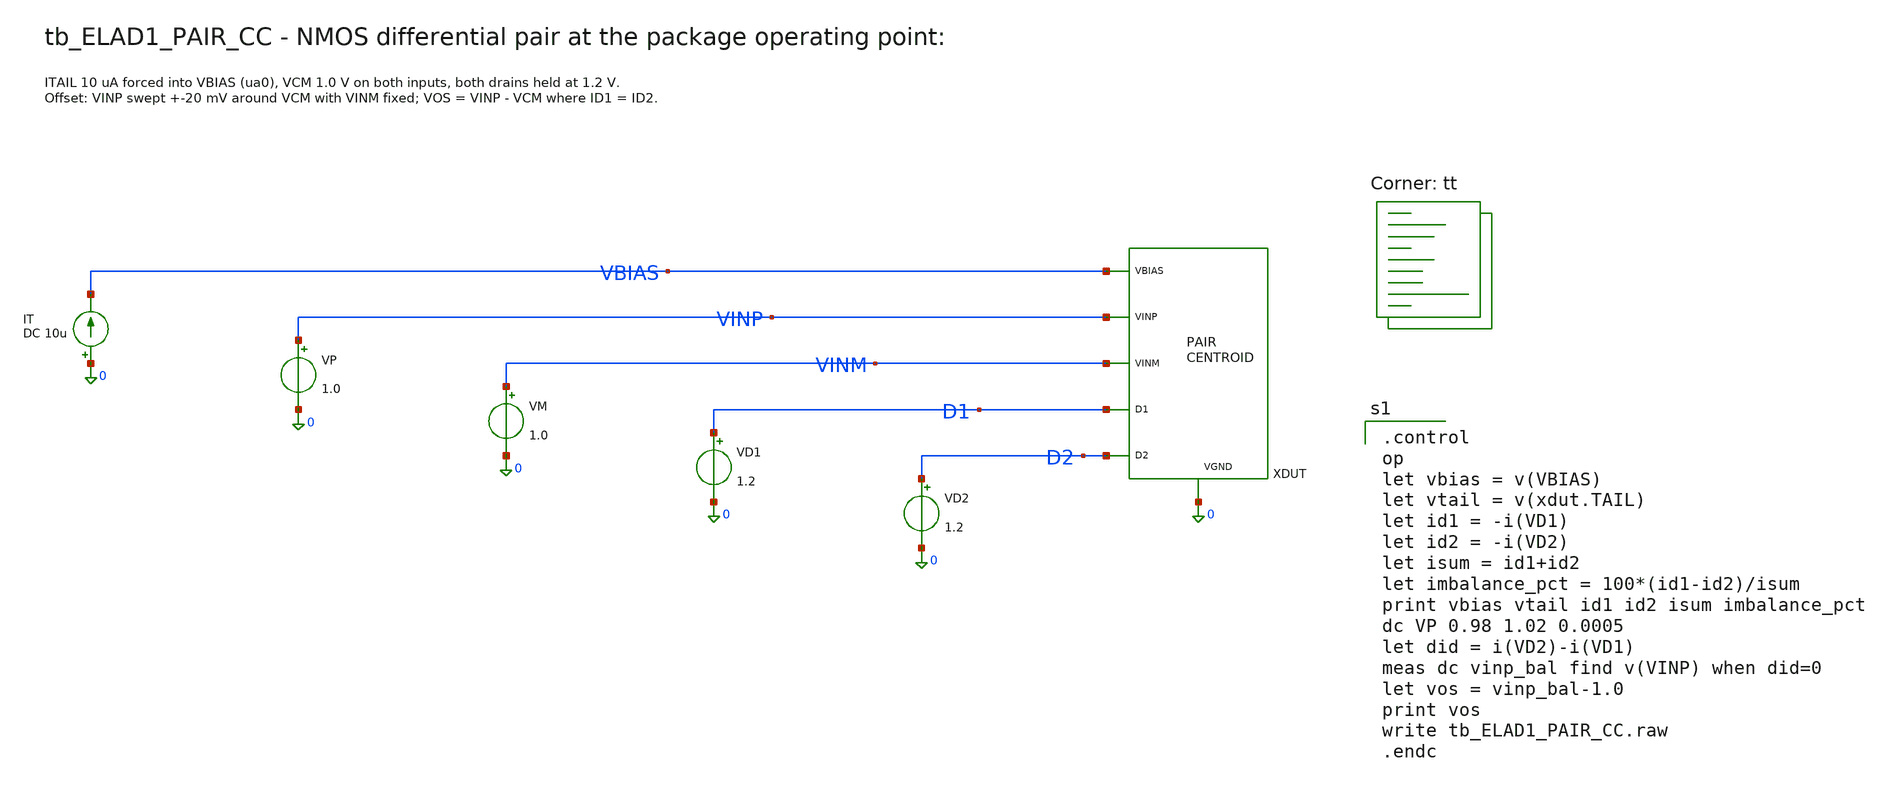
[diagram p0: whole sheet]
** sch_path: cells/ELAD1_PAIR_CC/schematic/tb_ELAD1_PAIR_CC.sch
**.subckt tb_ELAD1_PAIR_CC
XDUT VINP VINM D1 D2 VBIAS 0 ELAD1_PAIR_CC
VD2 D2 0 1.2
VD1 D1 0 1.2
VM VINM 0 1.0
VP VINP 0 1.0
IT 0 VBIAS DC 10u
**** begin user architecture code

.control
op
let vbias = v(VBIAS)
let vtail = v(xdut.TAIL)
let id1 = -i(VD1)
let id2 = -i(VD2)
let isum = id1+id2
let imbalance_pct = 100*(id1-id2)/isum
print vbias vtail id1 id2 isum imbalance_pct
dc VP 0.98 1.02 0.0005
let did = i(VD2)-i(VD1)
meas dc vinp_bal find v(VINP) when did=0
let vos = vinp_bal-1.0
print vos
write tb_ELAD1_PAIR_CC.raw
.endc

.lib $::SKYWATER_MODELS/sky130.lib.spice tt
**** end user architecture code
**.ends

* expanding   symbol:  ELAD1_PAIR_CC.sym # of pins=6
** sym_path: cells/ELAD1_PAIR_CC/schematic/ELAD1_PAIR_CC.sym
** sch_path: cells/ELAD1_PAIR_CC/schematic/ELAD1_PAIR_CC.sch
.subckt ELAD1_PAIR_CC VINP VINM D1 D2 VBIAS VGND
*.iopin D1
*.iopin D2
*.iopin VINP
*.iopin VINM
*.iopin VBIAS
*.iopin VGND
XA[3] D1 VINP TAIL VGND sky130_fd_pr__nfet_01v8 L=1 W=2 nf=1 ad='int((1 + 1)/2) * 2 / 1 * 0.29' as='int((1 + 2)/2) * 2 / 1 * 0.29'
+ pd='2*int((1 + 1)/2) * (2 / 1 + 0.29)' ps='2*int((1 + 2)/2) * (2 / 1 + 0.29)' nrd='0.29 / 2 ' nrs='0.29 / 2 '
+ sa=0 sb=0 sd=0 mult=1 m=1
XA[2] D1 VINP TAIL VGND sky130_fd_pr__nfet_01v8 L=1 W=2 nf=1 ad='int((1 + 1)/2) * 2 / 1 * 0.29' as='int((1 + 2)/2) * 2 / 1 * 0.29'
+ pd='2*int((1 + 1)/2) * (2 / 1 + 0.29)' ps='2*int((1 + 2)/2) * (2 / 1 + 0.29)' nrd='0.29 / 2 ' nrs='0.29 / 2 '
+ sa=0 sb=0 sd=0 mult=1 m=1
XA[1] D1 VINP TAIL VGND sky130_fd_pr__nfet_01v8 L=1 W=2 nf=1 ad='int((1 + 1)/2) * 2 / 1 * 0.29' as='int((1 + 2)/2) * 2 / 1 * 0.29'
+ pd='2*int((1 + 1)/2) * (2 / 1 + 0.29)' ps='2*int((1 + 2)/2) * (2 / 1 + 0.29)' nrd='0.29 / 2 ' nrs='0.29 / 2 '
+ sa=0 sb=0 sd=0 mult=1 m=1
XA[0] D1 VINP TAIL VGND sky130_fd_pr__nfet_01v8 L=1 W=2 nf=1 ad='int((1 + 1)/2) * 2 / 1 * 0.29' as='int((1 + 2)/2) * 2 / 1 * 0.29'
+ pd='2*int((1 + 1)/2) * (2 / 1 + 0.29)' ps='2*int((1 + 2)/2) * (2 / 1 + 0.29)' nrd='0.29 / 2 ' nrs='0.29 / 2 '
+ sa=0 sb=0 sd=0 mult=1 m=1
XB[3] D2 VINM TAIL VGND sky130_fd_pr__nfet_01v8 L=1 W=2 nf=1 ad='int((1 + 1)/2) * 2 / 1 * 0.29' as='int((1 + 2)/2) * 2 / 1 * 0.29'
+ pd='2*int((1 + 1)/2) * (2 / 1 + 0.29)' ps='2*int((1 + 2)/2) * (2 / 1 + 0.29)' nrd='0.29 / 2 ' nrs='0.29 / 2 '
+ sa=0 sb=0 sd=0 mult=1 m=1
XB[2] D2 VINM TAIL VGND sky130_fd_pr__nfet_01v8 L=1 W=2 nf=1 ad='int((1 + 1)/2) * 2 / 1 * 0.29' as='int((1 + 2)/2) * 2 / 1 * 0.29'
+ pd='2*int((1 + 1)/2) * (2 / 1 + 0.29)' ps='2*int((1 + 2)/2) * (2 / 1 + 0.29)' nrd='0.29 / 2 ' nrs='0.29 / 2 '
+ sa=0 sb=0 sd=0 mult=1 m=1
XB[1] D2 VINM TAIL VGND sky130_fd_pr__nfet_01v8 L=1 W=2 nf=1 ad='int((1 + 1)/2) * 2 / 1 * 0.29' as='int((1 + 2)/2) * 2 / 1 * 0.29'
+ pd='2*int((1 + 1)/2) * (2 / 1 + 0.29)' ps='2*int((1 + 2)/2) * (2 / 1 + 0.29)' nrd='0.29 / 2 ' nrs='0.29 / 2 '
+ sa=0 sb=0 sd=0 mult=1 m=1
XB[0] D2 VINM TAIL VGND sky130_fd_pr__nfet_01v8 L=1 W=2 nf=1 ad='int((1 + 1)/2) * 2 / 1 * 0.29' as='int((1 + 2)/2) * 2 / 1 * 0.29'
+ pd='2*int((1 + 1)/2) * (2 / 1 + 0.29)' ps='2*int((1 + 2)/2) * (2 / 1 + 0.29)' nrd='0.29 / 2 ' nrs='0.29 / 2 '
+ sa=0 sb=0 sd=0 mult=1 m=1
XT[3] TAIL VBIAS VGND VGND sky130_fd_pr__nfet_01v8 L=1 W=2 nf=1 ad='int((1 + 1)/2) * 2 / 1 * 0.29' as='int((1 + 2)/2) * 2 / 1 * 0.29'
+ pd='2*int((1 + 1)/2) * (2 / 1 + 0.29)' ps='2*int((1 + 2)/2) * (2 / 1 + 0.29)' nrd='0.29 / 2 ' nrs='0.29 / 2 '
+ sa=0 sb=0 sd=0 mult=1 m=1
XT[2] TAIL VBIAS VGND VGND sky130_fd_pr__nfet_01v8 L=1 W=2 nf=1 ad='int((1 + 1)/2) * 2 / 1 * 0.29' as='int((1 + 2)/2) * 2 / 1 * 0.29'
+ pd='2*int((1 + 1)/2) * (2 / 1 + 0.29)' ps='2*int((1 + 2)/2) * (2 / 1 + 0.29)' nrd='0.29 / 2 ' nrs='0.29 / 2 '
+ sa=0 sb=0 sd=0 mult=1 m=1
XT[1] TAIL VBIAS VGND VGND sky130_fd_pr__nfet_01v8 L=1 W=2 nf=1 ad='int((1 + 1)/2) * 2 / 1 * 0.29' as='int((1 + 2)/2) * 2 / 1 * 0.29'
+ pd='2*int((1 + 1)/2) * (2 / 1 + 0.29)' ps='2*int((1 + 2)/2) * (2 / 1 + 0.29)' nrd='0.29 / 2 ' nrs='0.29 / 2 '
+ sa=0 sb=0 sd=0 mult=1 m=1
XT[0] TAIL VBIAS VGND VGND sky130_fd_pr__nfet_01v8 L=1 W=2 nf=1 ad='int((1 + 1)/2) * 2 / 1 * 0.29' as='int((1 + 2)/2) * 2 / 1 * 0.29'
+ pd='2*int((1 + 1)/2) * (2 / 1 + 0.29)' ps='2*int((1 + 2)/2) * (2 / 1 + 0.29)' nrd='0.29 / 2 ' nrs='0.29 / 2 '
+ sa=0 sb=0 sd=0 mult=1 m=1
XR[3] VBIAS VBIAS VGND VGND sky130_fd_pr__nfet_01v8 L=1 W=2 nf=1 ad='int((1 + 1)/2) * 2 / 1 * 0.29' as='int((1 + 2)/2) * 2 / 1 * 0.29'
+ pd='2*int((1 + 1)/2) * (2 / 1 + 0.29)' ps='2*int((1 + 2)/2) * (2 / 1 + 0.29)' nrd='0.29 / 2 ' nrs='0.29 / 2 '
+ sa=0 sb=0 sd=0 mult=1 m=1
XR[2] VBIAS VBIAS VGND VGND sky130_fd_pr__nfet_01v8 L=1 W=2 nf=1 ad='int((1 + 1)/2) * 2 / 1 * 0.29' as='int((1 + 2)/2) * 2 / 1 * 0.29'
+ pd='2*int((1 + 1)/2) * (2 / 1 + 0.29)' ps='2*int((1 + 2)/2) * (2 / 1 + 0.29)' nrd='0.29 / 2 ' nrs='0.29 / 2 '
+ sa=0 sb=0 sd=0 mult=1 m=1
XR[1] VBIAS VBIAS VGND VGND sky130_fd_pr__nfet_01v8 L=1 W=2 nf=1 ad='int((1 + 1)/2) * 2 / 1 * 0.29' as='int((1 + 2)/2) * 2 / 1 * 0.29'
+ pd='2*int((1 + 1)/2) * (2 / 1 + 0.29)' ps='2*int((1 + 2)/2) * (2 / 1 + 0.29)' nrd='0.29 / 2 ' nrs='0.29 / 2 '
+ sa=0 sb=0 sd=0 mult=1 m=1
XR[0] VBIAS VBIAS VGND VGND sky130_fd_pr__nfet_01v8 L=1 W=2 nf=1 ad='int((1 + 1)/2) * 2 / 1 * 0.29' as='int((1 + 2)/2) * 2 / 1 * 0.29'
+ pd='2*int((1 + 1)/2) * (2 / 1 + 0.29)' ps='2*int((1 + 2)/2) * (2 / 1 + 0.29)' nrd='0.29 / 2 ' nrs='0.29 / 2 '
+ sa=0 sb=0 sd=0 mult=1 m=1
XDUM[31] VGND VGND VGND VGND sky130_fd_pr__nfet_01v8 L=1 W=2 nf=1 ad='int((1 + 1)/2) * 2 / 1 * 0.29'
+ as='int((1 + 2)/2) * 2 / 1 * 0.29' pd='2*int((1 + 1)/2) * (2 / 1 + 0.29)' ps='2*int((1 + 2)/2) * (2 / 1 + 0.29)'
+ nrd='0.29 / 2 ' nrs='0.29 / 2 ' sa=0 sb=0 sd=0 mult=1 m=1
XDUM[30] VGND VGND VGND VGND sky130_fd_pr__nfet_01v8 L=1 W=2 nf=1 ad='int((1 + 1)/2) * 2 / 1 * 0.29'
+ as='int((1 + 2)/2) * 2 / 1 * 0.29' pd='2*int((1 + 1)/2) * (2 / 1 + 0.29)' ps='2*int((1 + 2)/2) * (2 / 1 + 0.29)'
+ nrd='0.29 / 2 ' nrs='0.29 / 2 ' sa=0 sb=0 sd=0 mult=1 m=1
XDUM[29] VGND VGND VGND VGND sky130_fd_pr__nfet_01v8 L=1 W=2 nf=1 ad='int((1 + 1)/2) * 2 / 1 * 0.29'
+ as='int((1 + 2)/2) * 2 / 1 * 0.29' pd='2*int((1 + 1)/2) * (2 / 1 + 0.29)' ps='2*int((1 + 2)/2) * (2 / 1 + 0.29)'
+ nrd='0.29 / 2 ' nrs='0.29 / 2 ' sa=0 sb=0 sd=0 mult=1 m=1
XDUM[28] VGND VGND VGND VGND sky130_fd_pr__nfet_01v8 L=1 W=2 nf=1 ad='int((1 + 1)/2) * 2 / 1 * 0.29'
+ as='int((1 + 2)/2) * 2 / 1 * 0.29' pd='2*int((1 + 1)/2) * (2 / 1 + 0.29)' ps='2*int((1 + 2)/2) * (2 / 1 + 0.29)'
+ nrd='0.29 / 2 ' nrs='0.29 / 2 ' sa=0 sb=0 sd=0 mult=1 m=1
XDUM[27] VGND VGND VGND VGND sky130_fd_pr__nfet_01v8 L=1 W=2 nf=1 ad='int((1 + 1)/2) * 2 / 1 * 0.29'
+ as='int((1 + 2)/2) * 2 / 1 * 0.29' pd='2*int((1 + 1)/2) * (2 / 1 + 0.29)' ps='2*int((1 + 2)/2) * (2 / 1 + 0.29)'
+ nrd='0.29 / 2 ' nrs='0.29 / 2 ' sa=0 sb=0 sd=0 mult=1 m=1
XDUM[26] VGND VGND VGND VGND sky130_fd_pr__nfet_01v8 L=1 W=2 nf=1 ad='int((1 + 1)/2) * 2 / 1 * 0.29'
+ as='int((1 + 2)/2) * 2 / 1 * 0.29' pd='2*int((1 + 1)/2) * (2 / 1 + 0.29)' ps='2*int((1 + 2)/2) * (2 / 1 + 0.29)'
+ nrd='0.29 / 2 ' nrs='0.29 / 2 ' sa=0 sb=0 sd=0 mult=1 m=1
XDUM[25] VGND VGND VGND VGND sky130_fd_pr__nfet_01v8 L=1 W=2 nf=1 ad='int((1 + 1)/2) * 2 / 1 * 0.29'
+ as='int((1 + 2)/2) * 2 / 1 * 0.29' pd='2*int((1 + 1)/2) * (2 / 1 + 0.29)' ps='2*int((1 + 2)/2) * (2 / 1 + 0.29)'
+ nrd='0.29 / 2 ' nrs='0.29 / 2 ' sa=0 sb=0 sd=0 mult=1 m=1
XDUM[24] VGND VGND VGND VGND sky130_fd_pr__nfet_01v8 L=1 W=2 nf=1 ad='int((1 + 1)/2) * 2 / 1 * 0.29'
+ as='int((1 + 2)/2) * 2 / 1 * 0.29' pd='2*int((1 + 1)/2) * (2 / 1 + 0.29)' ps='2*int((1 + 2)/2) * (2 / 1 + 0.29)'
+ nrd='0.29 / 2 ' nrs='0.29 / 2 ' sa=0 sb=0 sd=0 mult=1 m=1
XDUM[23] VGND VGND VGND VGND sky130_fd_pr__nfet_01v8 L=1 W=2 nf=1 ad='int((1 + 1)/2) * 2 / 1 * 0.29'
+ as='int((1 + 2)/2) * 2 / 1 * 0.29' pd='2*int((1 + 1)/2) * (2 / 1 + 0.29)' ps='2*int((1 + 2)/2) * (2 / 1 + 0.29)'
+ nrd='0.29 / 2 ' nrs='0.29 / 2 ' sa=0 sb=0 sd=0 mult=1 m=1
XDUM[22] VGND VGND VGND VGND sky130_fd_pr__nfet_01v8 L=1 W=2 nf=1 ad='int((1 + 1)/2) * 2 / 1 * 0.29'
+ as='int((1 + 2)/2) * 2 / 1 * 0.29' pd='2*int((1 + 1)/2) * (2 / 1 + 0.29)' ps='2*int((1 + 2)/2) * (2 / 1 + 0.29)'
+ nrd='0.29 / 2 ' nrs='0.29 / 2 ' sa=0 sb=0 sd=0 mult=1 m=1
XDUM[21] VGND VGND VGND VGND sky130_fd_pr__nfet_01v8 L=1 W=2 nf=1 ad='int((1 + 1)/2) * 2 / 1 * 0.29'
+ as='int((1 + 2)/2) * 2 / 1 * 0.29' pd='2*int((1 + 1)/2) * (2 / 1 + 0.29)' ps='2*int((1 + 2)/2) * (2 / 1 + 0.29)'
+ nrd='0.29 / 2 ' nrs='0.29 / 2 ' sa=0 sb=0 sd=0 mult=1 m=1
XDUM[20] VGND VGND VGND VGND sky130_fd_pr__nfet_01v8 L=1 W=2 nf=1 ad='int((1 + 1)/2) * 2 / 1 * 0.29'
+ as='int((1 + 2)/2) * 2 / 1 * 0.29' pd='2*int((1 + 1)/2) * (2 / 1 + 0.29)' ps='2*int((1 + 2)/2) * (2 / 1 + 0.29)'
+ nrd='0.29 / 2 ' nrs='0.29 / 2 ' sa=0 sb=0 sd=0 mult=1 m=1
XDUM[19] VGND VGND VGND VGND sky130_fd_pr__nfet_01v8 L=1 W=2 nf=1 ad='int((1 + 1)/2) * 2 / 1 * 0.29'
+ as='int((1 + 2)/2) * 2 / 1 * 0.29' pd='2*int((1 + 1)/2) * (2 / 1 + 0.29)' ps='2*int((1 + 2)/2) * (2 / 1 + 0.29)'
+ nrd='0.29 / 2 ' nrs='0.29 / 2 ' sa=0 sb=0 sd=0 mult=1 m=1
XDUM[18] VGND VGND VGND VGND sky130_fd_pr__nfet_01v8 L=1 W=2 nf=1 ad='int((1 + 1)/2) * 2 / 1 * 0.29'
+ as='int((1 + 2)/2) * 2 / 1 * 0.29' pd='2*int((1 + 1)/2) * (2 / 1 + 0.29)' ps='2*int((1 + 2)/2) * (2 / 1 + 0.29)'
+ nrd='0.29 / 2 ' nrs='0.29 / 2 ' sa=0 sb=0 sd=0 mult=1 m=1
XDUM[17] VGND VGND VGND VGND sky130_fd_pr__nfet_01v8 L=1 W=2 nf=1 ad='int((1 + 1)/2) * 2 / 1 * 0.29'
+ as='int((1 + 2)/2) * 2 / 1 * 0.29' pd='2*int((1 + 1)/2) * (2 / 1 + 0.29)' ps='2*int((1 + 2)/2) * (2 / 1 + 0.29)'
+ nrd='0.29 / 2 ' nrs='0.29 / 2 ' sa=0 sb=0 sd=0 mult=1 m=1
XDUM[16] VGND VGND VGND VGND sky130_fd_pr__nfet_01v8 L=1 W=2 nf=1 ad='int((1 + 1)/2) * 2 / 1 * 0.29'
+ as='int((1 + 2)/2) * 2 / 1 * 0.29' pd='2*int((1 + 1)/2) * (2 / 1 + 0.29)' ps='2*int((1 + 2)/2) * (2 / 1 + 0.29)'
+ nrd='0.29 / 2 ' nrs='0.29 / 2 ' sa=0 sb=0 sd=0 mult=1 m=1
XDUM[15] VGND VGND VGND VGND sky130_fd_pr__nfet_01v8 L=1 W=2 nf=1 ad='int((1 + 1)/2) * 2 / 1 * 0.29'
+ as='int((1 + 2)/2) * 2 / 1 * 0.29' pd='2*int((1 + 1)/2) * (2 / 1 + 0.29)' ps='2*int((1 + 2)/2) * (2 / 1 + 0.29)'
+ nrd='0.29 / 2 ' nrs='0.29 / 2 ' sa=0 sb=0 sd=0 mult=1 m=1
XDUM[14] VGND VGND VGND VGND sky130_fd_pr__nfet_01v8 L=1 W=2 nf=1 ad='int((1 + 1)/2) * 2 / 1 * 0.29'
+ as='int((1 + 2)/2) * 2 / 1 * 0.29' pd='2*int((1 + 1)/2) * (2 / 1 + 0.29)' ps='2*int((1 + 2)/2) * (2 / 1 + 0.29)'
+ nrd='0.29 / 2 ' nrs='0.29 / 2 ' sa=0 sb=0 sd=0 mult=1 m=1
XDUM[13] VGND VGND VGND VGND sky130_fd_pr__nfet_01v8 L=1 W=2 nf=1 ad='int((1 + 1)/2) * 2 / 1 * 0.29'
+ as='int((1 + 2)/2) * 2 / 1 * 0.29' pd='2*int((1 + 1)/2) * (2 / 1 + 0.29)' ps='2*int((1 + 2)/2) * (2 / 1 + 0.29)'
+ nrd='0.29 / 2 ' nrs='0.29 / 2 ' sa=0 sb=0 sd=0 mult=1 m=1
XDUM[12] VGND VGND VGND VGND sky130_fd_pr__nfet_01v8 L=1 W=2 nf=1 ad='int((1 + 1)/2) * 2 / 1 * 0.29'
+ as='int((1 + 2)/2) * 2 / 1 * 0.29' pd='2*int((1 + 1)/2) * (2 / 1 + 0.29)' ps='2*int((1 + 2)/2) * (2 / 1 + 0.29)'
+ nrd='0.29 / 2 ' nrs='0.29 / 2 ' sa=0 sb=0 sd=0 mult=1 m=1
XDUM[11] VGND VGND VGND VGND sky130_fd_pr__nfet_01v8 L=1 W=2 nf=1 ad='int((1 + 1)/2) * 2 / 1 * 0.29'
+ as='int((1 + 2)/2) * 2 / 1 * 0.29' pd='2*int((1 + 1)/2) * (2 / 1 + 0.29)' ps='2*int((1 + 2)/2) * (2 / 1 + 0.29)'
+ nrd='0.29 / 2 ' nrs='0.29 / 2 ' sa=0 sb=0 sd=0 mult=1 m=1
XDUM[10] VGND VGND VGND VGND sky130_fd_pr__nfet_01v8 L=1 W=2 nf=1 ad='int((1 + 1)/2) * 2 / 1 * 0.29'
+ as='int((1 + 2)/2) * 2 / 1 * 0.29' pd='2*int((1 + 1)/2) * (2 / 1 + 0.29)' ps='2*int((1 + 2)/2) * (2 / 1 + 0.29)'
+ nrd='0.29 / 2 ' nrs='0.29 / 2 ' sa=0 sb=0 sd=0 mult=1 m=1
XDUM[9] VGND VGND VGND VGND sky130_fd_pr__nfet_01v8 L=1 W=2 nf=1 ad='int((1 + 1)/2) * 2 / 1 * 0.29' as='int((1 + 2)/2) * 2 / 1 * 0.29'
+ pd='2*int((1 + 1)/2) * (2 / 1 + 0.29)' ps='2*int((1 + 2)/2) * (2 / 1 + 0.29)' nrd='0.29 / 2 ' nrs='0.29 / 2 '
+ sa=0 sb=0 sd=0 mult=1 m=1
XDUM[8] VGND VGND VGND VGND sky130_fd_pr__nfet_01v8 L=1 W=2 nf=1 ad='int((1 + 1)/2) * 2 / 1 * 0.29' as='int((1 + 2)/2) * 2 / 1 * 0.29'
+ pd='2*int((1 + 1)/2) * (2 / 1 + 0.29)' ps='2*int((1 + 2)/2) * (2 / 1 + 0.29)' nrd='0.29 / 2 ' nrs='0.29 / 2 '
+ sa=0 sb=0 sd=0 mult=1 m=1
XDUM[7] VGND VGND VGND VGND sky130_fd_pr__nfet_01v8 L=1 W=2 nf=1 ad='int((1 + 1)/2) * 2 / 1 * 0.29' as='int((1 + 2)/2) * 2 / 1 * 0.29'
+ pd='2*int((1 + 1)/2) * (2 / 1 + 0.29)' ps='2*int((1 + 2)/2) * (2 / 1 + 0.29)' nrd='0.29 / 2 ' nrs='0.29 / 2 '
+ sa=0 sb=0 sd=0 mult=1 m=1
XDUM[6] VGND VGND VGND VGND sky130_fd_pr__nfet_01v8 L=1 W=2 nf=1 ad='int((1 + 1)/2) * 2 / 1 * 0.29' as='int((1 + 2)/2) * 2 / 1 * 0.29'
+ pd='2*int((1 + 1)/2) * (2 / 1 + 0.29)' ps='2*int((1 + 2)/2) * (2 / 1 + 0.29)' nrd='0.29 / 2 ' nrs='0.29 / 2 '
+ sa=0 sb=0 sd=0 mult=1 m=1
XDUM[5] VGND VGND VGND VGND sky130_fd_pr__nfet_01v8 L=1 W=2 nf=1 ad='int((1 + 1)/2) * 2 / 1 * 0.29' as='int((1 + 2)/2) * 2 / 1 * 0.29'
+ pd='2*int((1 + 1)/2) * (2 / 1 + 0.29)' ps='2*int((1 + 2)/2) * (2 / 1 + 0.29)' nrd='0.29 / 2 ' nrs='0.29 / 2 '
+ sa=0 sb=0 sd=0 mult=1 m=1
XDUM[4] VGND VGND VGND VGND sky130_fd_pr__nfet_01v8 L=1 W=2 nf=1 ad='int((1 + 1)/2) * 2 / 1 * 0.29' as='int((1 + 2)/2) * 2 / 1 * 0.29'
+ pd='2*int((1 + 1)/2) * (2 / 1 + 0.29)' ps='2*int((1 + 2)/2) * (2 / 1 + 0.29)' nrd='0.29 / 2 ' nrs='0.29 / 2 '
+ sa=0 sb=0 sd=0 mult=1 m=1
XDUM[3] VGND VGND VGND VGND sky130_fd_pr__nfet_01v8 L=1 W=2 nf=1 ad='int((1 + 1)/2) * 2 / 1 * 0.29' as='int((1 + 2)/2) * 2 / 1 * 0.29'
+ pd='2*int((1 + 1)/2) * (2 / 1 + 0.29)' ps='2*int((1 + 2)/2) * (2 / 1 + 0.29)' nrd='0.29 / 2 ' nrs='0.29 / 2 '
+ sa=0 sb=0 sd=0 mult=1 m=1
XDUM[2] VGND VGND VGND VGND sky130_fd_pr__nfet_01v8 L=1 W=2 nf=1 ad='int((1 + 1)/2) * 2 / 1 * 0.29' as='int((1 + 2)/2) * 2 / 1 * 0.29'
+ pd='2*int((1 + 1)/2) * (2 / 1 + 0.29)' ps='2*int((1 + 2)/2) * (2 / 1 + 0.29)' nrd='0.29 / 2 ' nrs='0.29 / 2 '
+ sa=0 sb=0 sd=0 mult=1 m=1
XDUM[1] VGND VGND VGND VGND sky130_fd_pr__nfet_01v8 L=1 W=2 nf=1 ad='int((1 + 1)/2) * 2 / 1 * 0.29' as='int((1 + 2)/2) * 2 / 1 * 0.29'
+ pd='2*int((1 + 1)/2) * (2 / 1 + 0.29)' ps='2*int((1 + 2)/2) * (2 / 1 + 0.29)' nrd='0.29 / 2 ' nrs='0.29 / 2 '
+ sa=0 sb=0 sd=0 mult=1 m=1
XDUM[0] VGND VGND VGND VGND sky130_fd_pr__nfet_01v8 L=1 W=2 nf=1 ad='int((1 + 1)/2) * 2 / 1 * 0.29' as='int((1 + 2)/2) * 2 / 1 * 0.29'
+ pd='2*int((1 + 1)/2) * (2 / 1 + 0.29)' ps='2*int((1 + 2)/2) * (2 / 1 + 0.29)' nrd='0.29 / 2 ' nrs='0.29 / 2 '
+ sa=0 sb=0 sd=0 mult=1 m=1
.ends

.end
